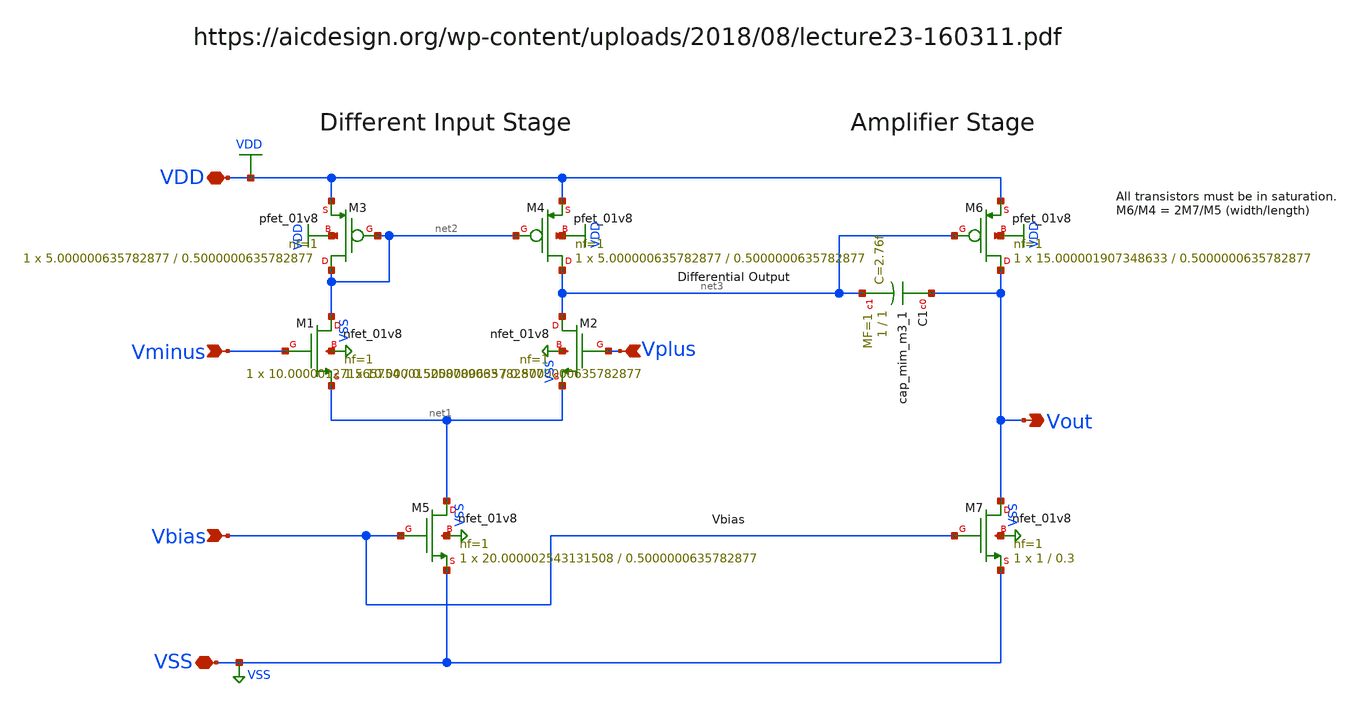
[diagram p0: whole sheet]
** sch_path: examples/template/OpAmp.sch
**.subckt OpAmp Vplus Vminus VDD VSS Vbias Vout
*.ipin Vplus
*.ipin Vminus
*.iopin VDD
*.iopin VSS
*.ipin Vbias
*.opin Vout
XM1 net2 Vminus net1 VSS sky130_fd_pr__nfet_01v8 L=0.5000000635782877 W=10.000015258789063 nf=1 ad='int((nf+1)/2) * W/nf * 0.29'
+ as='int((nf+2)/2) * W/nf * 0.29' pd='2*int((nf+1)/2) * (W/nf + 0.29)' ps='2*int((nf+2)/2) * (W/nf + 0.29)'
+ nrd='0.29 / W' nrs='0.29 / W' sa=0 sb=0 sd=0 mult=1 m=1
XM2 net3 Vplus net1 VSS sky130_fd_pr__nfet_01v8 L=0.5000000635782877 W=10.000001271565754 nf=1 ad='int((nf+1)/2) * W/nf * 0.29'
+ as='int((nf+2)/2) * W/nf * 0.29' pd='2*int((nf+1)/2) * (W/nf + 0.29)' ps='2*int((nf+2)/2) * (W/nf + 0.29)'
+ nrd='0.29 / W' nrs='0.29 / W' sa=0 sb=0 sd=0 mult=1 m=1
XM3 net2 net2 VDD VDD sky130_fd_pr__pfet_01v8 L=0.5000000635782877 W=5.000000635782877 nf=1 ad='int((nf+1)/2) * W/nf * 0.29'
+ as='int((nf+2)/2) * W/nf * 0.29' pd='2*int((nf+1)/2) * (W/nf + 0.29)' ps='2*int((nf+2)/2) * (W/nf + 0.29)'
+ nrd='0.29 / W' nrs='0.29 / W' sa=0 sb=0 sd=0 mult=1 m=1
XM4 net3 net2 VDD VDD sky130_fd_pr__pfet_01v8 L=0.5000000635782877 W=5.000000635782877 nf=1 ad='int((nf+1)/2) * W/nf * 0.29'
+ as='int((nf+2)/2) * W/nf * 0.29' pd='2*int((nf+1)/2) * (W/nf + 0.29)' ps='2*int((nf+2)/2) * (W/nf + 0.29)'
+ nrd='0.29 / W' nrs='0.29 / W' sa=0 sb=0 sd=0 mult=1 m=1
XM5 net1 Vbias VSS VSS sky130_fd_pr__nfet_01v8 L=0.5000000635782877 W=20.000002543131508 nf=1 ad='int((nf+1)/2) * W/nf * 0.29'
+ as='int((nf+2)/2) * W/nf * 0.29' pd='2*int((nf+1)/2) * (W/nf + 0.29)' ps='2*int((nf+2)/2) * (W/nf + 0.29)'
+ nrd='0.29 / W' nrs='0.29 / W' sa=0 sb=0 sd=0 mult=1 m=1
XM6 Vout net3 VDD VDD sky130_fd_pr__pfet_01v8 L=0.5000000635782877 W=15.000001907348633 nf=1 ad='int((nf+1)/2) * W/nf * 0.29'
+ as='int((nf+2)/2) * W/nf * 0.29' pd='2*int((nf+1)/2) * (W/nf + 0.29)' ps='2*int((nf+2)/2) * (W/nf + 0.29)'
+ nrd='0.29 / W' nrs='0.29 / W' sa=0 sb=0 sd=0 mult=1 m=1
XC1 Vout net3 sky130_fd_pr__cap_mim_m3_1 W=1 L=1 MF=1 m=1
XM7 Vout Vbias VSS VSS sky130_fd_pr__nfet_01v8 L=0.3 W=1 nf=1 ad='int((nf+1)/2) * W/nf * 0.29' as='int((nf+2)/2) * W/nf * 0.29'
+ pd='2*int((nf+1)/2) * (W/nf + 0.29)' ps='2*int((nf+2)/2) * (W/nf + 0.29)' nrd='0.29 / W' nrs='0.29 / W'
+ sa=0 sb=0 sd=0 mult=1 m=1
**.ends
.GLOBAL VDD
.GLOBAL VSS
.end
